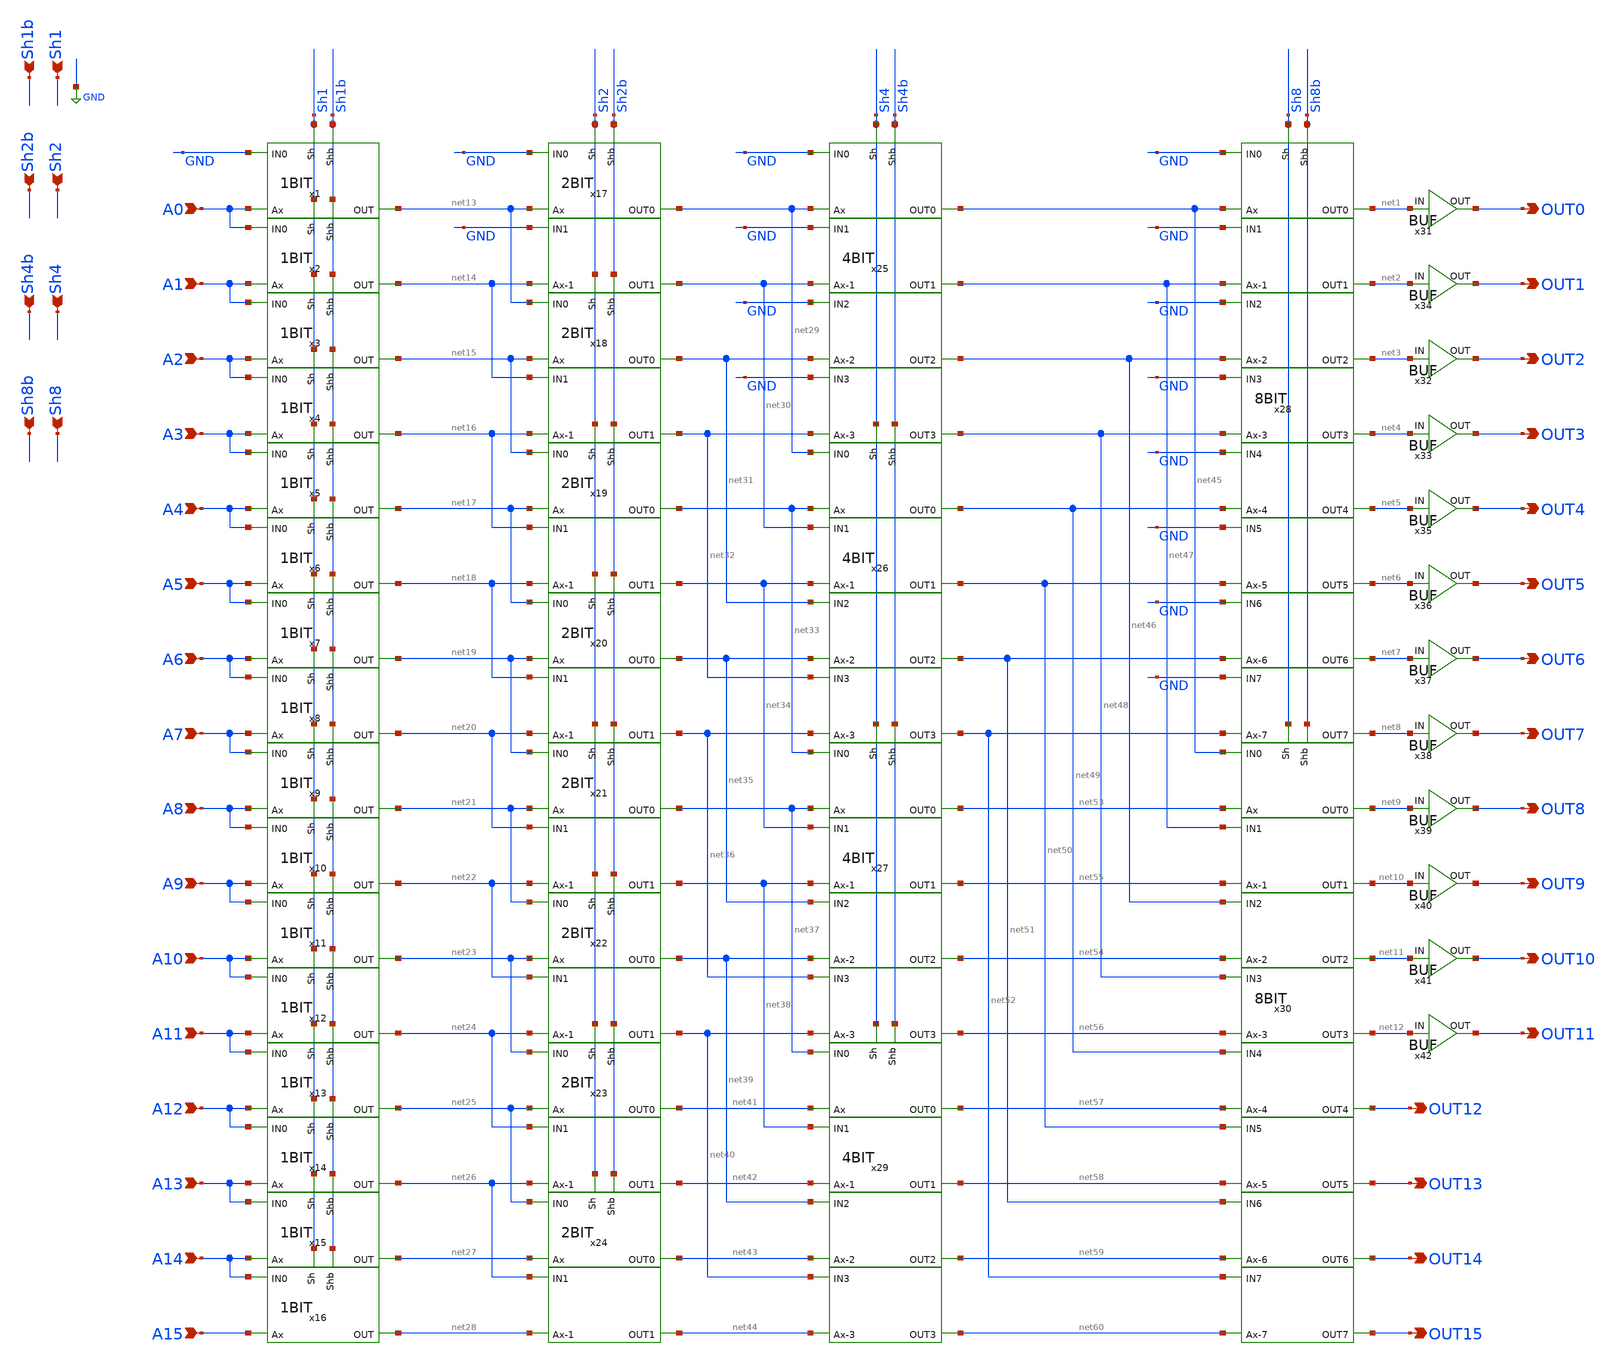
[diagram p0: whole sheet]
** sch_path: SHIFT.sch
**.subckt SHIFT Sh1 Sh1b A0 A1 A2 A3 A4 A5 A6 A7 A8 A9 A10 A11 A12 A13 A14 A15 OUT0 OUT1 OUT2 OUT3
*+ OUT4 OUT5 OUT6 OUT7 OUT8 OUT9 OUT10 OUT11 OUT12 OUT13 OUT14 OUT15 Sh2 Sh2b Sh4 Sh4b Sh8 Sh8b
*.ipin Sh1
*.ipin Sh1b
*.ipin A0
*.ipin A1
*.ipin A2
*.ipin A3
*.ipin A4
*.ipin A5
*.ipin A6
*.ipin A7
*.ipin A8
*.ipin A9
*.ipin A10
*.ipin A11
*.ipin A12
*.ipin A13
*.ipin A14
*.ipin A15
*.opin OUT0
*.opin OUT1
*.opin OUT2
*.opin OUT3
*.opin OUT4
*.opin OUT5
*.opin OUT6
*.opin OUT7
*.opin OUT8
*.opin OUT9
*.opin OUT10
*.opin OUT11
*.opin OUT12
*.opin OUT13
*.opin OUT14
*.opin OUT15
*.ipin Sh2
*.ipin Sh2b
*.ipin Sh4
*.ipin Sh4b
*.ipin Sh8
*.ipin Sh8b
x1 Sh1b Sh1 A0 GND net13 1BIT
x2 Sh1b Sh1 A1 A0 net14 1BIT
x3 Sh1b Sh1 A2 A1 net15 1BIT
x4 Sh1b Sh1 A3 A2 net16 1BIT
x5 Sh1b Sh1 A4 A3 net17 1BIT
x6 Sh1b Sh1 A5 A4 net18 1BIT
x7 Sh1b Sh1 A6 A5 net19 1BIT
x8 Sh1b Sh1 A7 A6 net20 1BIT
x9 Sh1b Sh1 A8 A7 net21 1BIT
x10 Sh1b Sh1 A9 A8 net22 1BIT
x11 Sh1b Sh1 A10 A9 net23 1BIT
x12 Sh1b Sh1 A11 A10 net24 1BIT
x13 Sh1b Sh1 A12 A11 net25 1BIT
x14 Sh1b Sh1 A13 A12 net26 1BIT
x15 Sh1b Sh1 A14 A13 net27 1BIT
x16 Sh1b Sh1 A15 A14 net28 1BIT
x17 Sh2b Sh2 net13 GND net29 net30 GND net14 2BIT
x18 Sh2b Sh2 net15 net13 net31 net32 net14 net16 2BIT
x19 Sh2b Sh2 net17 net15 net33 net34 net16 net18 2BIT
x20 Sh2b Sh2 net19 net17 net35 net36 net18 net20 2BIT
x21 Sh2b Sh2 net21 net19 net37 net38 net20 net22 2BIT
x22 Sh2b Sh2 net23 net21 net39 net40 net22 net24 2BIT
x23 Sh2b Sh2 net25 net23 net41 net42 net24 net26 2BIT
x24 Sh2b Sh2 net27 net25 net43 net44 net26 net28 2BIT
x25 Sh4b Sh4 GND net29 net45 net47 net46 net48 GND net30 GND net31 GND net32 4BIT
x26 Sh4b Sh4 net29 net33 net49 net50 net51 net52 net30 net34 net31 net35 net32 net36 4BIT
x27 Sh4b Sh4 net33 net37 net53 net55 net54 net56 net34 net38 net35 net39 net36 net40 4BIT
x29 Sh4b Sh4 net37 net41 net57 net58 net59 net60 net38 net42 net39 net43 net40 net44 4BIT
x28 Sh8b Sh8 net45 GND net1 net2 net3 net4 net47 GND GND net46 GND net48 net49 GND net5 net6 net7
+ net8 GND net50 GND net51 GND net52 8BIT
x30 Sh8b Sh8 net53 net45 net9 net10 net11 net12 net55 net47 net46 net54 net48 net56 net57 net49
+ OUT12 OUT13 OUT14 OUT15 net50 net58 net51 net59 net52 net60 8BIT
x31 OUT0 net1 BUF
x32 OUT2 net3 BUF
x33 OUT3 net4 BUF
x34 OUT1 net2 BUF
x35 OUT4 net5 BUF
x36 OUT5 net6 BUF
x37 OUT6 net7 BUF
x38 OUT7 net8 BUF
x39 OUT8 net9 BUF
x40 OUT9 net10 BUF
x41 OUT10 net11 BUF
x42 OUT11 net12 BUF
**.ends
.GLOBAL GND
.end
